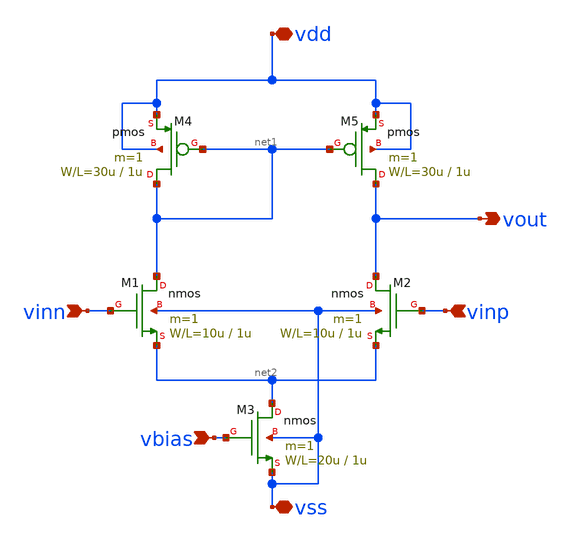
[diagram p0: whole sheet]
** sch_path: diff.sch
**.subckt diff vss vdd vinn vinp vout vbias
*.iopin vss
*.iopin vdd
*.ipin vinn
*.ipin vinp
*.opin vout
*.ipin vbias
M1 net1 vinn net2 vss nmos L=1u W=10u m=1
M2 vout vinp net2 vss nmos L=1u W=10u m=1
M3 net2 vbias vss vss nmos L=1u W=20u m=1
M4 net1 net1 vdd vdd pmos L=1u W=30u m=1
M5 vout net1 vdd vdd pmos L=1u W=30u m=1
**** begin user architecture code
 .include $::LIB/mos.lib
.include $::LIB/passive.lib
.include $::LIB/diode.lib
**** end user architecture code
**.ends
.end
